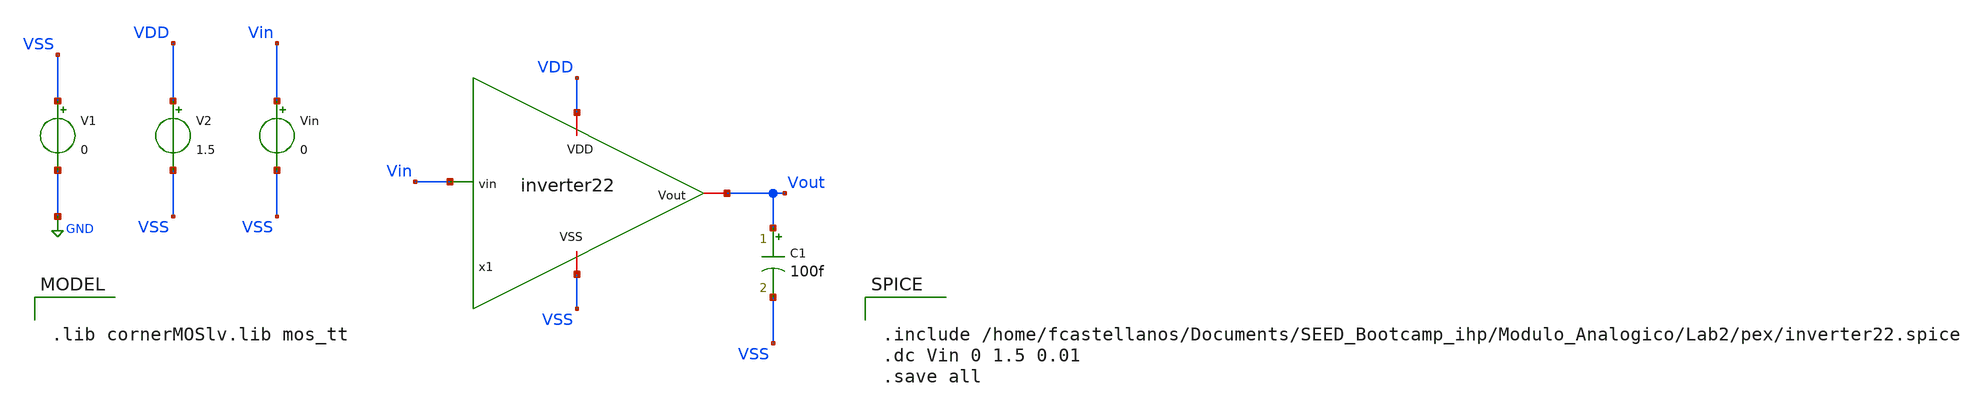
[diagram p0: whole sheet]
** sch_path: Lab2/pex/inverter_tb.sch
**.subckt inverter_tb
C1 Vout VSS 100f m=1
V1 VSS GND 0
V2 VDD VSS 1.5
Vin Vin VSS 0
x1 VDD Vin Vout VSS inverter22
**** begin user architecture code


.include /home/fcastellanos/Documents/SEED_Bootcamp_ihp/Modulo_Analogico/Lab2/pex/inverter22.spice
.dc Vin 0 1.5 0.01
.save all



.lib cornerMOSlv.lib mos_tt

**** end user architecture code
**.ends
.GLOBAL GND
.end
